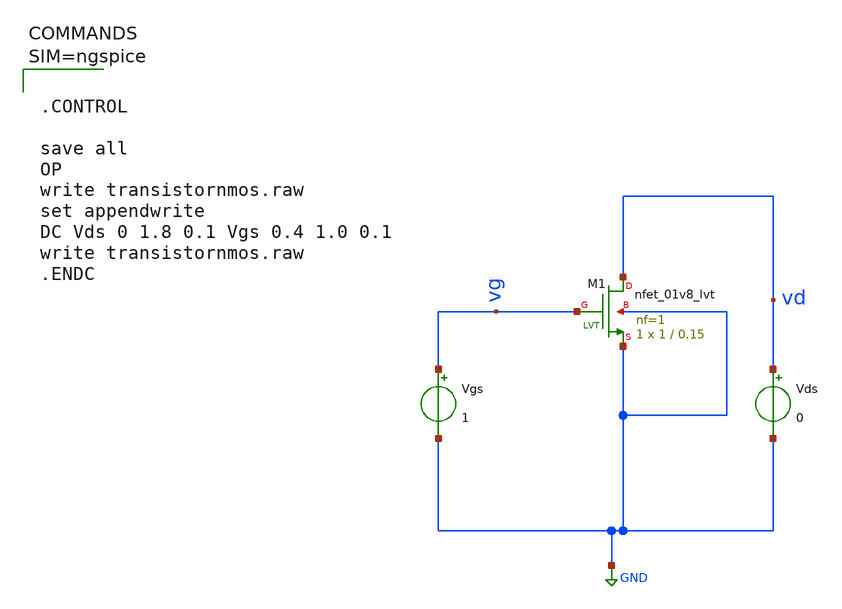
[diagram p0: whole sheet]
** sch_path: work/xschem/transistornmos.sch
**.subckt transistornmos
Vgs vg GND 1
Vds vd GND 0
XM1 vd vg GND GND sky130_fd_pr__nfet_01v8_lvt L=0.15 W=1 nf=1 ad='int((1 + 1)/2) * 1 / 1 * 0.29' as='int((1 + 2)/2) * 1 / 1 * 0.29'
+ pd='2*int((1 + 1)/2) * (1 / 1 + 0.29)' ps='2*int((1 + 2)/2) * (1 / 1 + 0.29)' nrd='0.29 / 1 ' nrs='0.29 / 1 '
+ sa=0 sb=0 sd=0 mult=1 m=1
**** begin user architecture code



.CONTROL

save all
OP
write transistornmos.raw
set appendwrite
DC Vds 0 1.8 0.1 Vgs 0.4 1.0 0.1
write transistornmos.raw
.ENDC




** opencircuitdesign pdks install
.lib $::SKYWATER_MODELS/sky130.lib.spice tt

**** end user architecture code
**.ends
.GLOBAL GND
.end
